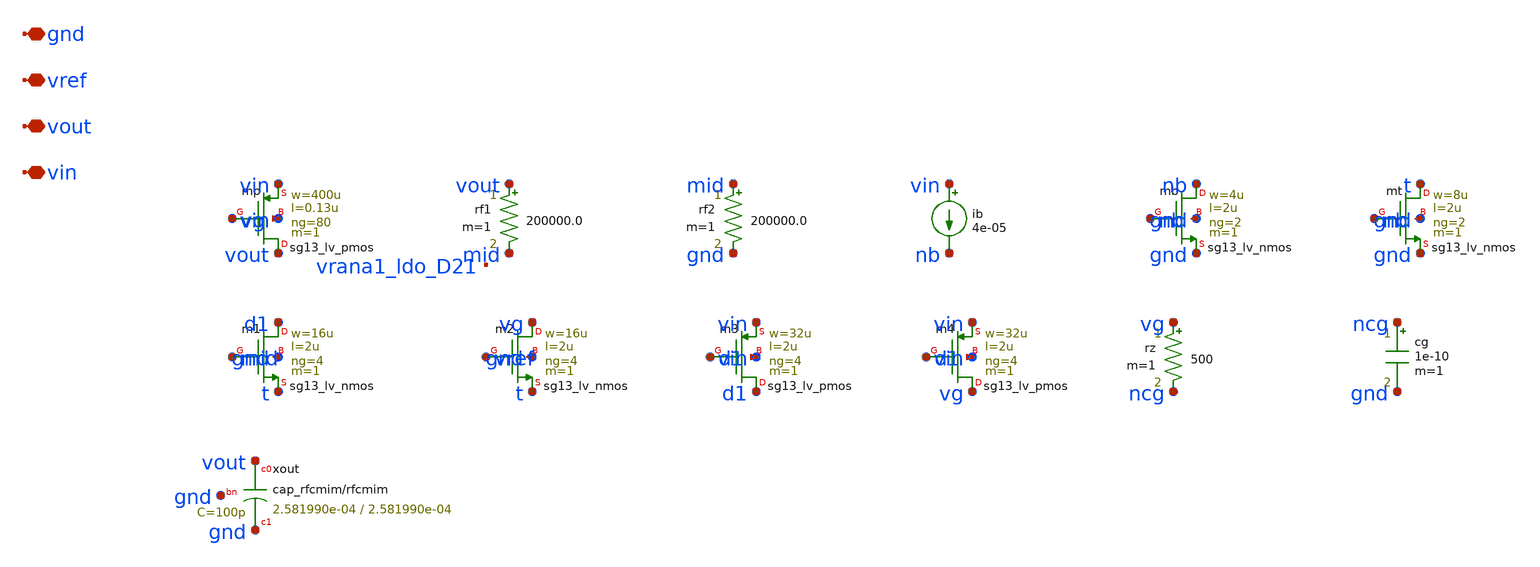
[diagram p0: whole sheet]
** sch_path: analog/vco/sch/vrana1_ldo.sch
**.subckt vrana1_ldo vin vout vref gnd
*.iopin vin
*.iopin vout
*.iopin vref
*.iopin gnd
Xmp vout vg vin vin sg13_lv_pmos w=400u l=0.13u ng=80 m=1 mm_ok=1
rf1 vout mid 200000.0 m=1
rf2 mid gnd 200000.0 m=1
ib vin nb 4e-05
Xmb nb nb gnd gnd sg13_lv_nmos w=4u l=2u ng=2 m=1 mm_ok=1
Xmt t nb gnd gnd sg13_lv_nmos w=8u l=2u ng=2 m=1 mm_ok=1
Xm1 d1 mid t gnd sg13_lv_nmos w=16u l=2u ng=4 m=1 mm_ok=1
Xm2 vg vref t gnd sg13_lv_nmos w=16u l=2u ng=4 m=1 mm_ok=1
Xm3 d1 d1 vin vin sg13_lv_pmos w=32u l=2u ng=4 m=1 mm_ok=1
Xm4 vg d1 vin vin sg13_lv_pmos w=32u l=2u ng=4 m=1 mm_ok=1
rz vg ncg 500 m=1
cg ncg gnd 1e-10 m=1
Xxout vout gnd gnd cap_rfcmim w=2.581990e-04 l=2.581990e-04 wfeed=5.0e-6 m=1 mm_ok=1
**.ends
.end
